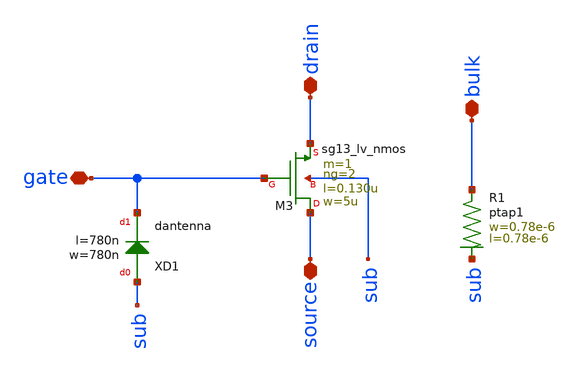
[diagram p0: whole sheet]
** sch_path: ts_pr_May2024/design_data/xschem/nmos2.sch
**.subckt nmos2 drain source bulk gate
*.iopin drain
*.iopin source
*.iopin bulk
*.iopin gate
XR1 bulk sub ptap1 R=262.8 w=0.78e-6 l=0.78e-6
XM3 source gate drain sub sg13_lv_nmos w=5u l=0.130u ng=2 m=1 mm_ok=1
XXD1 sub gate dantenna l=780n w=780n
**.ends
.end
